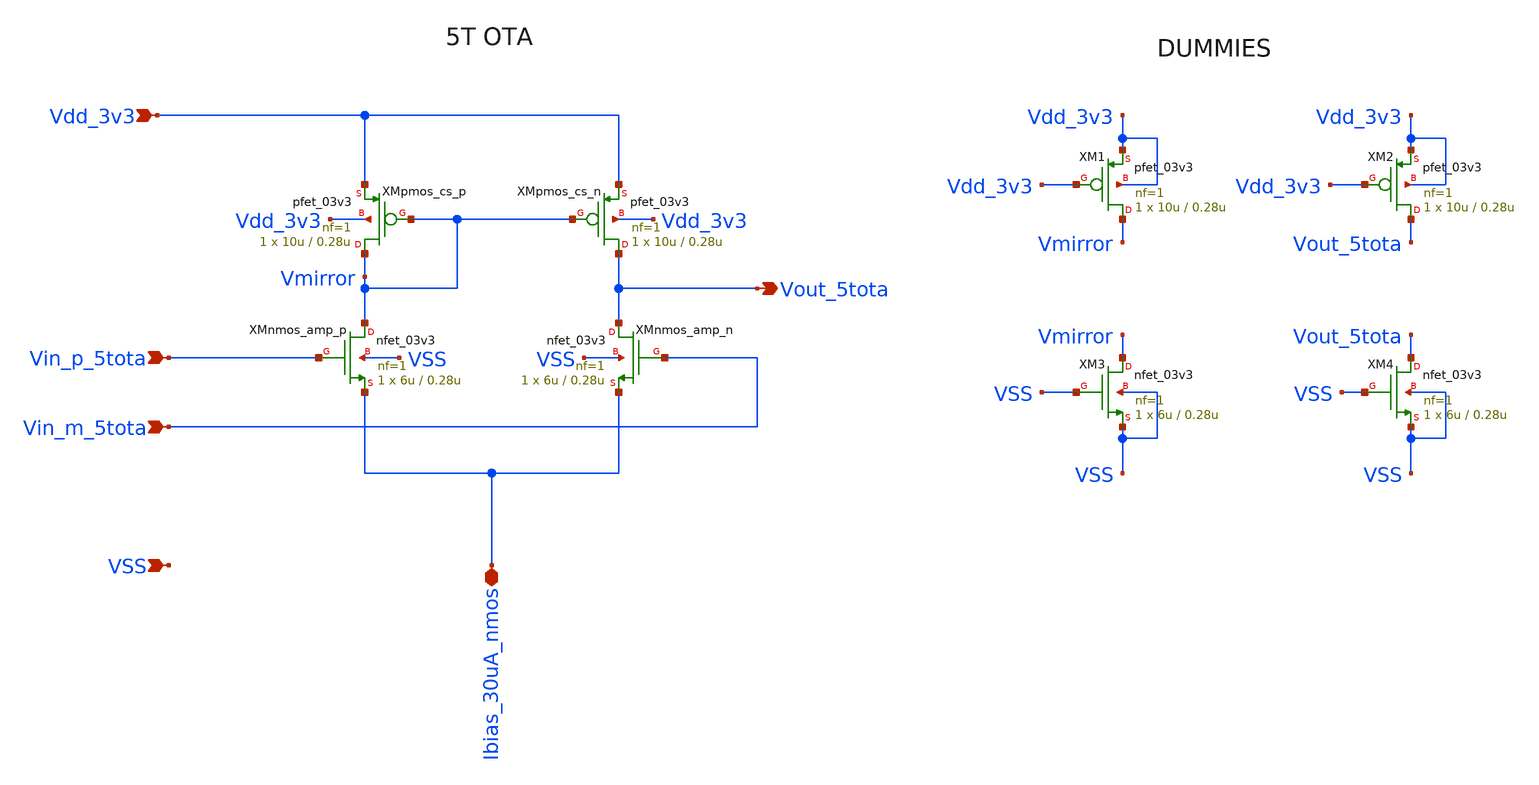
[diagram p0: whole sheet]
** sch_path: Analog/schematics/2_mixer/ota_5t.sch
**.subckt ota_5t Vdd_3v3 Vin_p_5tota Vin_m_5tota Vout_5tota Ibias_30uA_nmos VSS
*.ipin Vdd_3v3
*.ipin Vin_p_5tota
*.ipin Vin_m_5tota
*.opin Vout_5tota
*.iopin Ibias_30uA_nmos
*.ipin VSS
XMnmos_amp_p Vmirror Vin_p_5tota Ibias_30uA_nmos VSS nfet_03v3 L=0.28u W=6u nf=1 ad='int((nf+1)/2) * W/nf * 0.18u'
+ as='int((nf+2)/2) * W/nf * 0.18u' pd='2*int((nf+1)/2) * (W/nf + 0.18u)' ps='2*int((nf+2)/2) * (W/nf + 0.18u)'
+ nrd='0.18u / W' nrs='0.18u / W' sa=0 sb=0 sd=0 m=1
XMnmos_amp_n Vout_5tota Vin_m_5tota Ibias_30uA_nmos VSS nfet_03v3 L=0.28u W=6u nf=1 ad='int((nf+1)/2) * W/nf * 0.18u'
+ as='int((nf+2)/2) * W/nf * 0.18u' pd='2*int((nf+1)/2) * (W/nf + 0.18u)' ps='2*int((nf+2)/2) * (W/nf + 0.18u)'
+ nrd='0.18u / W' nrs='0.18u / W' sa=0 sb=0 sd=0 m=1
XMpmos_cs_p Vmirror Vmirror Vdd_3v3 Vdd_3v3 pfet_03v3 L=0.28u W=10u nf=1 ad='int((nf+1)/2) * W/nf * 0.18u'
+ as='int((nf+2)/2) * W/nf * 0.18u' pd='2*int((nf+1)/2) * (W/nf + 0.18u)' ps='2*int((nf+2)/2) * (W/nf + 0.18u)'
+ nrd='0.18u / W' nrs='0.18u / W' sa=0 sb=0 sd=0 m=1
XMpmos_cs_n Vout_5tota Vmirror Vdd_3v3 Vdd_3v3 pfet_03v3 L=0.28u W=10u nf=1 ad='int((nf+1)/2) * W/nf * 0.18u'
+ as='int((nf+2)/2) * W/nf * 0.18u' pd='2*int((nf+1)/2) * (W/nf + 0.18u)' ps='2*int((nf+2)/2) * (W/nf + 0.18u)'
+ nrd='0.18u / W' nrs='0.18u / W' sa=0 sb=0 sd=0 m=1
XM1 Vmirror Vdd_3v3 Vdd_3v3 Vdd_3v3 pfet_03v3 L=0.28u W=10u nf=1 ad='int((nf+1)/2) * W/nf * 0.18u' as='int((nf+2)/2) * W/nf * 0.18u'
+ pd='2*int((nf+1)/2) * (W/nf + 0.18u)' ps='2*int((nf+2)/2) * (W/nf + 0.18u)' nrd='0.18u / W' nrs='0.18u / W'
+ sa=0 sb=0 sd=0 m=1
XM2 Vout_5tota Vdd_3v3 Vdd_3v3 Vdd_3v3 pfet_03v3 L=0.28u W=10u nf=1 ad='int((nf+1)/2) * W/nf * 0.18u'
+ as='int((nf+2)/2) * W/nf * 0.18u' pd='2*int((nf+1)/2) * (W/nf + 0.18u)' ps='2*int((nf+2)/2) * (W/nf + 0.18u)'
+ nrd='0.18u / W' nrs='0.18u / W' sa=0 sb=0 sd=0 m=1
XM3 Vmirror VSS VSS VSS nfet_03v3 L=0.28u W=6u nf=1 ad='int((nf+1)/2) * W/nf * 0.18u' as='int((nf+2)/2) * W/nf * 0.18u'
+ pd='2*int((nf+1)/2) * (W/nf + 0.18u)' ps='2*int((nf+2)/2) * (W/nf + 0.18u)' nrd='0.18u / W' nrs='0.18u / W'
+ sa=0 sb=0 sd=0 m=1
XM4 Vout_5tota VSS VSS VSS nfet_03v3 L=0.28u W=6u nf=1 ad='int((nf+1)/2) * W/nf * 0.18u' as='int((nf+2)/2) * W/nf * 0.18u'
+ pd='2*int((nf+1)/2) * (W/nf + 0.18u)' ps='2*int((nf+2)/2) * (W/nf + 0.18u)' nrd='0.18u / W' nrs='0.18u / W'
+ sa=0 sb=0 sd=0 m=1
**.ends
.end
